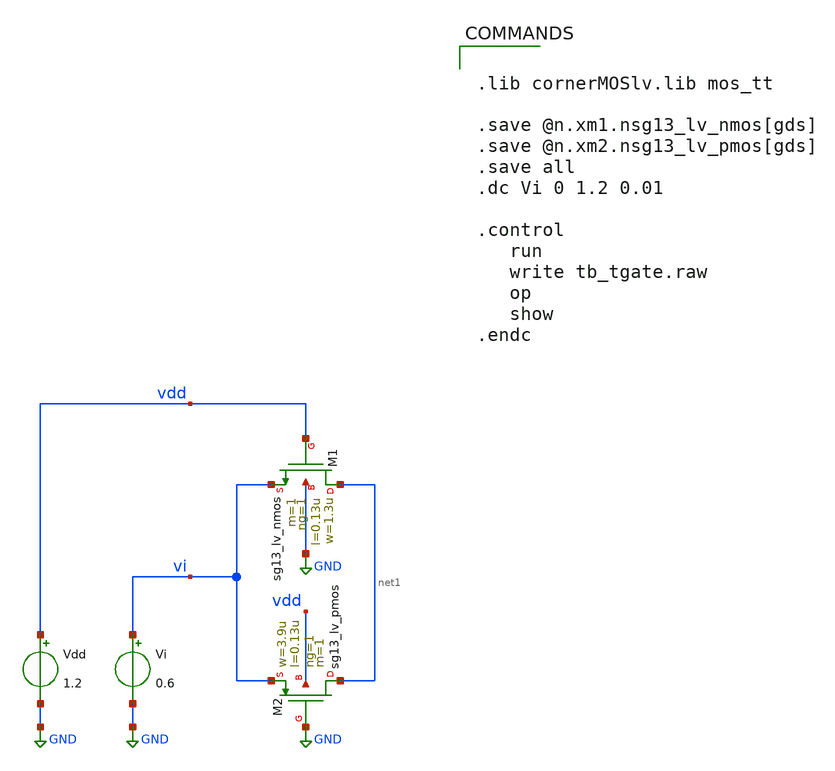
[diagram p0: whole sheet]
** sch_path: old/xschem/tb_tgate.sch
**.subckt tb_tgate
Vi vi GND 0.6
XM1 net1 vdd vi GND sg13_lv_nmos w=1.3u l=0.13u ng=1 m=1 mm_ok=1
XM2 net1 GND vi vdd sg13_lv_pmos w=3.9u l=0.13u ng=1 m=1 mm_ok=1
Vdd vdd GND 1.2
**** begin user architecture code


.lib cornerMOSlv.lib mos_tt

.save @n.xm1.nsg13_lv_nmos[gds]
.save @n.xm2.nsg13_lv_pmos[gds]
.save all
.dc Vi 0 1.2 0.01

.control
   run
   write tb_tgate.raw
   op
   show
.endc


**** end user architecture code
**.ends
.GLOBAL GND
.end
